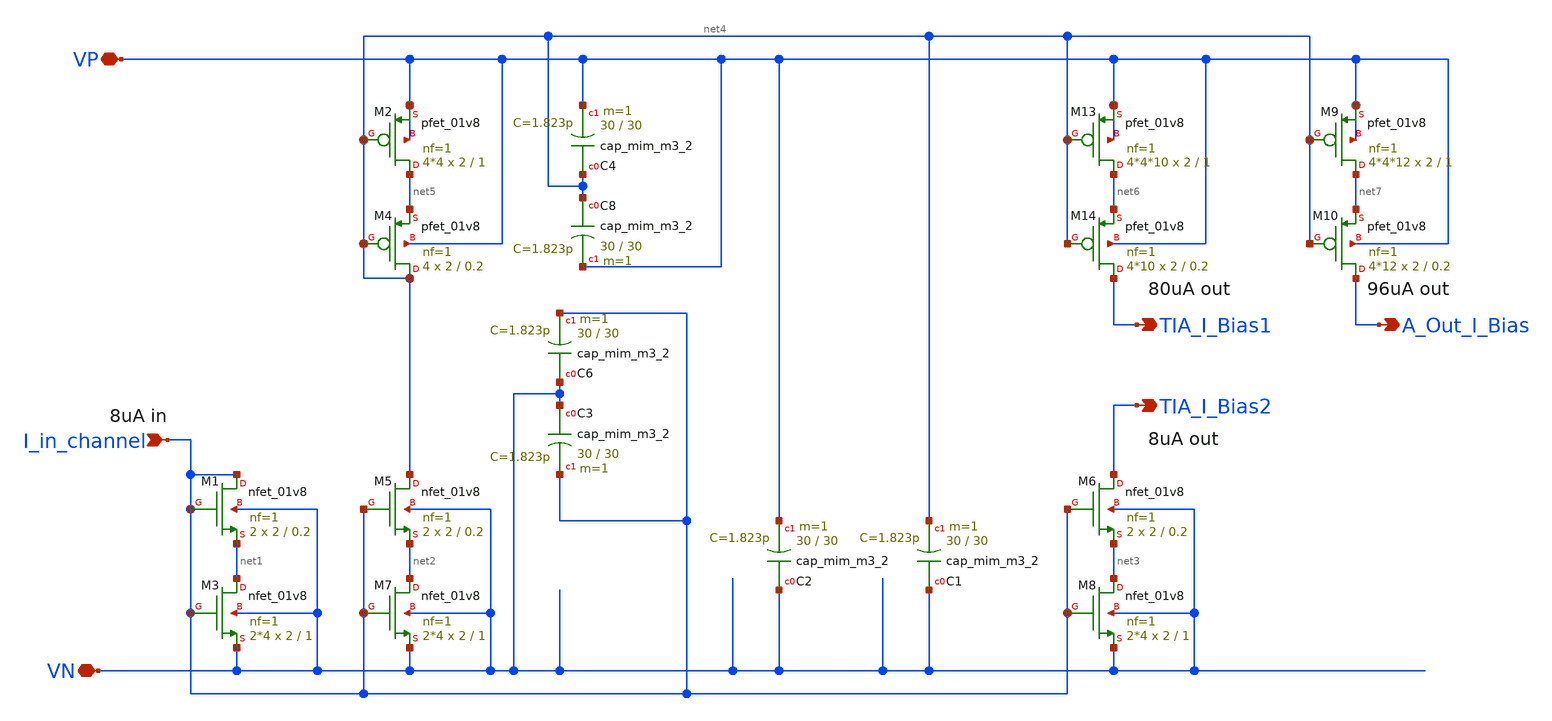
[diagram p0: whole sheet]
** sch_path: xschem/bias/current_mirror_channel.sch
**.subckt current_mirror_channel I_in_channel VP TIA_I_Bias2 VN TIA_I_Bias1 A_Out_I_Bias
*.ipin I_in_channel
*.iopin VP
*.opin TIA_I_Bias2
*.iopin VN
*.opin TIA_I_Bias1
*.opin A_Out_I_Bias
XM1 I_in_channel I_in_channel net1 VN sky130_fd_pr__nfet_01v8 L=0.2 W=2 nf=1 ad='int((nf+1)/2) * W/nf * 0.29'
+ as='int((nf+2)/2) * W/nf * 0.29' pd='2*int((nf+1)/2) * (W/nf + 0.29)' ps='2*int((nf+2)/2) * (W/nf + 0.29)'
+ nrd='0.29 / W' nrs='0.29 / W' sa=0 sb=0 sd=0 mult=2 m=2
XM2 net5 net4 VP VP sky130_fd_pr__pfet_01v8 L=1 W=2 nf=1 ad='int((nf+1)/2) * W/nf * 0.29' as='int((nf+2)/2) * W/nf * 0.29'
+ pd='2*int((nf+1)/2) * (W/nf + 0.29)' ps='2*int((nf+2)/2) * (W/nf + 0.29)' nrd='0.29 / W' nrs='0.29 / W'
+ sa=0 sb=0 sd=0 mult=4*4 m=4*4
XM3 net1 I_in_channel VN VN sky130_fd_pr__nfet_01v8 L=1 W=2 nf=1 ad='int((nf+1)/2) * W/nf * 0.29' as='int((nf+2)/2) * W/nf * 0.29'
+ pd='2*int((nf+1)/2) * (W/nf + 0.29)' ps='2*int((nf+2)/2) * (W/nf + 0.29)' nrd='0.29 / W' nrs='0.29 / W'
+ sa=0 sb=0 sd=0 mult=2*4 m=2*4
XM4 net4 net4 net5 VP sky130_fd_pr__pfet_01v8 L=0.2 W=2 nf=1 ad='int((nf+1)/2) * W/nf * 0.29' as='int((nf+2)/2) * W/nf * 0.29'
+ pd='2*int((nf+1)/2) * (W/nf + 0.29)' ps='2*int((nf+2)/2) * (W/nf + 0.29)' nrd='0.29 / W' nrs='0.29 / W'
+ sa=0 sb=0 sd=0 mult=4 m=4
XC8 net4 VP sky130_fd_pr__cap_mim_m3_2 W=30 L=30 MF=1 m=1
XM5 net4 I_in_channel net2 VN sky130_fd_pr__nfet_01v8 L=0.2 W=2 nf=1 ad='int((nf+1)/2) * W/nf * 0.29'
+ as='int((nf+2)/2) * W/nf * 0.29' pd='2*int((nf+1)/2) * (W/nf + 0.29)' ps='2*int((nf+2)/2) * (W/nf + 0.29)'
+ nrd='0.29 / W' nrs='0.29 / W' sa=0 sb=0 sd=0 mult=2 m=2
XM6 TIA_I_Bias2 I_in_channel net3 VN sky130_fd_pr__nfet_01v8 L=0.2 W=2 nf=1 ad='int((nf+1)/2) * W/nf * 0.29'
+ as='int((nf+2)/2) * W/nf * 0.29' pd='2*int((nf+1)/2) * (W/nf + 0.29)' ps='2*int((nf+2)/2) * (W/nf + 0.29)'
+ nrd='0.29 / W' nrs='0.29 / W' sa=0 sb=0 sd=0 mult=2 m=2
XM7 net2 I_in_channel VN VN sky130_fd_pr__nfet_01v8 L=1 W=2 nf=1 ad='int((nf+1)/2) * W/nf * 0.29' as='int((nf+2)/2) * W/nf * 0.29'
+ pd='2*int((nf+1)/2) * (W/nf + 0.29)' ps='2*int((nf+2)/2) * (W/nf + 0.29)' nrd='0.29 / W' nrs='0.29 / W'
+ sa=0 sb=0 sd=0 mult=2*4 m=2*4
XM8 net3 I_in_channel VN VN sky130_fd_pr__nfet_01v8 L=1 W=2 nf=1 ad='int((nf+1)/2) * W/nf * 0.29' as='int((nf+2)/2) * W/nf * 0.29'
+ pd='2*int((nf+1)/2) * (W/nf + 0.29)' ps='2*int((nf+2)/2) * (W/nf + 0.29)' nrd='0.29 / W' nrs='0.29 / W'
+ sa=0 sb=0 sd=0 mult=2*4 m=2*4
XM13 net6 net4 VP VP sky130_fd_pr__pfet_01v8 L=1 W=2 nf=1 ad='int((nf+1)/2) * W/nf * 0.29' as='int((nf+2)/2) * W/nf * 0.29'
+ pd='2*int((nf+1)/2) * (W/nf + 0.29)' ps='2*int((nf+2)/2) * (W/nf + 0.29)' nrd='0.29 / W' nrs='0.29 / W'
+ sa=0 sb=0 sd=0 mult=4*4*10 m=4*4*10
XM14 TIA_I_Bias1 net4 net6 VP sky130_fd_pr__pfet_01v8 L=0.2 W=2 nf=1 ad='int((nf+1)/2) * W/nf * 0.29'
+ as='int((nf+2)/2) * W/nf * 0.29' pd='2*int((nf+1)/2) * (W/nf + 0.29)' ps='2*int((nf+2)/2) * (W/nf + 0.29)'
+ nrd='0.29 / W' nrs='0.29 / W' sa=0 sb=0 sd=0 mult=4*10 m=4*10
XM9 net7 net4 VP VP sky130_fd_pr__pfet_01v8 L=1 W=2 nf=1 ad='int((nf+1)/2) * W/nf * 0.29' as='int((nf+2)/2) * W/nf * 0.29'
+ pd='2*int((nf+1)/2) * (W/nf + 0.29)' ps='2*int((nf+2)/2) * (W/nf + 0.29)' nrd='0.29 / W' nrs='0.29 / W'
+ sa=0 sb=0 sd=0 mult=4*4*12 m=4*4*12
XM10 A_Out_I_Bias net4 net7 VP sky130_fd_pr__pfet_01v8 L=0.2 W=2 nf=1 ad='int((nf+1)/2) * W/nf * 0.29'
+ as='int((nf+2)/2) * W/nf * 0.29' pd='2*int((nf+1)/2) * (W/nf + 0.29)' ps='2*int((nf+2)/2) * (W/nf + 0.29)'
+ nrd='0.29 / W' nrs='0.29 / W' sa=0 sb=0 sd=0 mult=4*12 m=4*12
XC4 net4 VP sky130_fd_pr__cap_mim_m3_2 W=30 L=30 MF=1 m=1
XC3 VN I_in_channel sky130_fd_pr__cap_mim_m3_2 W=30 L=30 MF=1 m=1
XC6 VN I_in_channel sky130_fd_pr__cap_mim_m3_2 W=30 L=30 MF=1 m=1
XC1 VN net4 sky130_fd_pr__cap_mim_m3_2 W=30 L=30 MF=1 m=1
XC2 VN VP sky130_fd_pr__cap_mim_m3_2 W=30 L=30 MF=1 m=1
**.ends
.end
